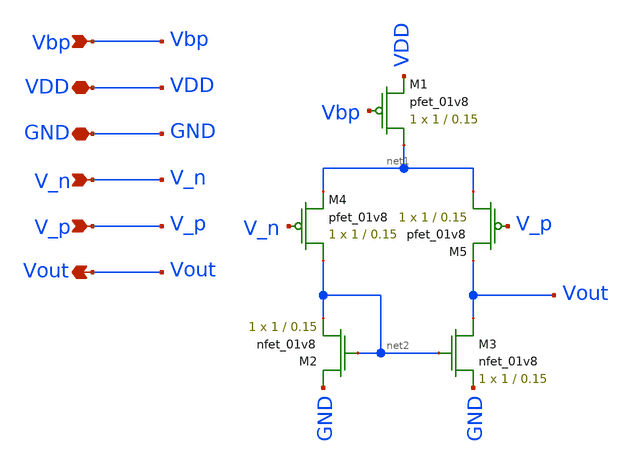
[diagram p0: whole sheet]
** sch_path: final/schematics/pmos_opamp.sch
**.subckt pmos_opamp VDD GND V_n V_p Vout Vbp
*.iopin VDD
*.iopin GND
*.ipin V_n
*.ipin V_p
*.opin Vout
*.ipin Vbp
XM1 net1 Vbp VDD VDD sky130_fd_pr__pfet_01v8 L=0.15 W=1 nf=1 ad='int((nf+1)/2) * W/nf * 0.29' as='int((nf+2)/2) * W/nf * 0.29'
+ pd='2*int((nf+1)/2) * (W/nf + 0.29)' ps='2*int((nf+2)/2) * (W/nf + 0.29)' nrd='0.29 / W' nrs='0.29 / W'
+ sa=0 sb=0 sd=0 mult=1 m=1
XM2 GND net2 net2 GND sky130_fd_pr__nfet_01v8 L=0.15 W=1 nf=1 ad='int((nf+1)/2) * W/nf * 0.29' as='int((nf+2)/2) * W/nf * 0.29'
+ pd='2*int((nf+1)/2) * (W/nf + 0.29)' ps='2*int((nf+2)/2) * (W/nf + 0.29)' nrd='0.29 / W' nrs='0.29 / W'
+ sa=0 sb=0 sd=0 mult=1 m=1
XM3 Vout net2 GND GND sky130_fd_pr__nfet_01v8 L=0.15 W=1 nf=1 ad='int((nf+1)/2) * W/nf * 0.29' as='int((nf+2)/2) * W/nf * 0.29'
+ pd='2*int((nf+1)/2) * (W/nf + 0.29)' ps='2*int((nf+2)/2) * (W/nf + 0.29)' nrd='0.29 / W' nrs='0.29 / W'
+ sa=0 sb=0 sd=0 mult=1 m=1
XM4 net2 V_n net1 VDD sky130_fd_pr__pfet_01v8 L=0.15 W=1 nf=1 ad='int((nf+1)/2) * W/nf * 0.29' as='int((nf+2)/2) * W/nf * 0.29'
+ pd='2*int((nf+1)/2) * (W/nf + 0.29)' ps='2*int((nf+2)/2) * (W/nf + 0.29)' nrd='0.29 / W' nrs='0.29 / W'
+ sa=0 sb=0 sd=0 mult=1 m=1
XM5 net1 V_p Vout VDD sky130_fd_pr__pfet_01v8 L=0.15 W=1 nf=1 ad='int((nf+1)/2) * W/nf * 0.29' as='int((nf+2)/2) * W/nf * 0.29'
+ pd='2*int((nf+1)/2) * (W/nf + 0.29)' ps='2*int((nf+2)/2) * (W/nf + 0.29)' nrd='0.29 / W' nrs='0.29 / W'
+ sa=0 sb=0 sd=0 mult=1 m=1
**.ends
.end
